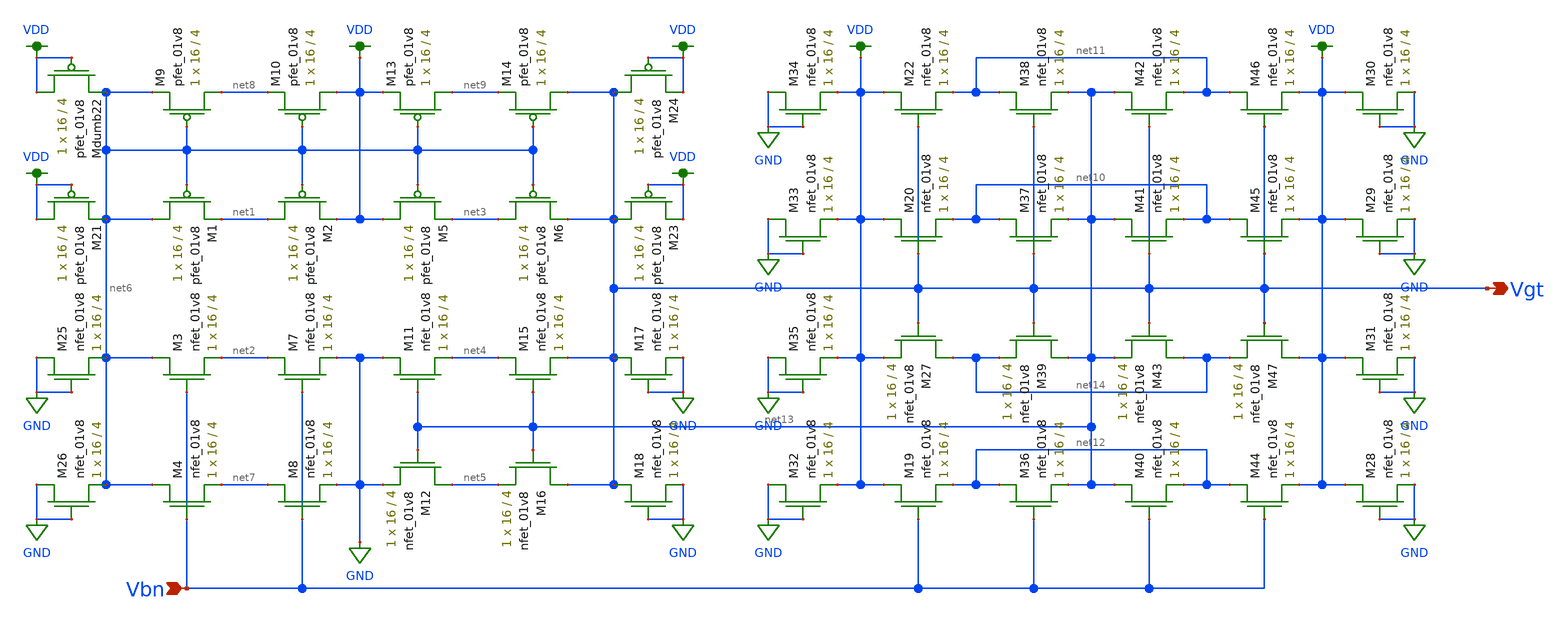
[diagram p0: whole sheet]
** sch_path: schematic/LDS/Vg_gen_lvs.sch
**.subckt Vg_gen_lvs Vbn Vgt
*.ipin Vbn
*.opin Vgt
XM1 net6 net6 net1 VDD sky130_fd_pr__pfet_01v8 L=4 W=16 nf=1 ad='int((nf+1)/2) * W/nf * 0.29' as='int((nf+2)/2) * W/nf * 0.29'
+ pd='2*int((nf+1)/2) * (W/nf + 0.29)' ps='2*int((nf+2)/2) * (W/nf + 0.29)' nrd='0.29 / W' nrs='0.29 / W'
+ sa=0 sb=0 sd=0 mult=1 m=1
XM2 net1 net6 VDD VDD sky130_fd_pr__pfet_01v8 L=4 W=16 nf=1 ad='int((nf+1)/2) * W/nf * 0.29' as='int((nf+2)/2) * W/nf * 0.29'
+ pd='2*int((nf+1)/2) * (W/nf + 0.29)' ps='2*int((nf+2)/2) * (W/nf + 0.29)' nrd='0.29 / W' nrs='0.29 / W'
+ sa=0 sb=0 sd=0 mult=1 m=1
XM5 VDD net6 net3 VDD sky130_fd_pr__pfet_01v8 L=4 W=16 nf=1 ad='int((nf+1)/2) * W/nf * 0.29' as='int((nf+2)/2) * W/nf * 0.29'
+ pd='2*int((nf+1)/2) * (W/nf + 0.29)' ps='2*int((nf+2)/2) * (W/nf + 0.29)' nrd='0.29 / W' nrs='0.29 / W'
+ sa=0 sb=0 sd=0 mult=1 m=1
XM6 net3 net6 Vgt VDD sky130_fd_pr__pfet_01v8 L=4 W=16 nf=1 ad='int((nf+1)/2) * W/nf * 0.29' as='int((nf+2)/2) * W/nf * 0.29'
+ pd='2*int((nf+1)/2) * (W/nf + 0.29)' ps='2*int((nf+2)/2) * (W/nf + 0.29)' nrd='0.29 / W' nrs='0.29 / W'
+ sa=0 sb=0 sd=0 mult=1 m=1
XM9 net8 net6 net6 VDD sky130_fd_pr__pfet_01v8 L=4 W=16 nf=1 ad='int((nf+1)/2) * W/nf * 0.29' as='int((nf+2)/2) * W/nf * 0.29'
+ pd='2*int((nf+1)/2) * (W/nf + 0.29)' ps='2*int((nf+2)/2) * (W/nf + 0.29)' nrd='0.29 / W' nrs='0.29 / W'
+ sa=0 sb=0 sd=0 mult=1 m=1
XM10 VDD net6 net8 VDD sky130_fd_pr__pfet_01v8 L=4 W=16 nf=1 ad='int((nf+1)/2) * W/nf * 0.29' as='int((nf+2)/2) * W/nf * 0.29'
+ pd='2*int((nf+1)/2) * (W/nf + 0.29)' ps='2*int((nf+2)/2) * (W/nf + 0.29)' nrd='0.29 / W' nrs='0.29 / W'
+ sa=0 sb=0 sd=0 mult=1 m=1
XM13 net9 net6 VDD VDD sky130_fd_pr__pfet_01v8 L=4 W=16 nf=1 ad='int((nf+1)/2) * W/nf * 0.29' as='int((nf+2)/2) * W/nf * 0.29'
+ pd='2*int((nf+1)/2) * (W/nf + 0.29)' ps='2*int((nf+2)/2) * (W/nf + 0.29)' nrd='0.29 / W' nrs='0.29 / W'
+ sa=0 sb=0 sd=0 mult=1 m=1
XM14 Vgt net6 net9 VDD sky130_fd_pr__pfet_01v8 L=4 W=16 nf=1 ad='int((nf+1)/2) * W/nf * 0.29' as='int((nf+2)/2) * W/nf * 0.29'
+ pd='2*int((nf+1)/2) * (W/nf + 0.29)' ps='2*int((nf+2)/2) * (W/nf + 0.29)' nrd='0.29 / W' nrs='0.29 / W'
+ sa=0 sb=0 sd=0 mult=1 m=1
XM21 VDD VDD net6 VDD sky130_fd_pr__pfet_01v8 L=4 W=16 nf=1 ad='int((nf+1)/2) * W/nf * 0.29' as='int((nf+2)/2) * W/nf * 0.29'
+ pd='2*int((nf+1)/2) * (W/nf + 0.29)' ps='2*int((nf+2)/2) * (W/nf + 0.29)' nrd='0.29 / W' nrs='0.29 / W'
+ sa=0 sb=0 sd=0 mult=1 m=1
XMdumb22 VDD VDD net6 VDD sky130_fd_pr__pfet_01v8 L=4 W=16 nf=1 ad='int((nf+1)/2) * W/nf * 0.29' as='int((nf+2)/2) * W/nf * 0.29'
+ pd='2*int((nf+1)/2) * (W/nf + 0.29)' ps='2*int((nf+2)/2) * (W/nf + 0.29)' nrd='0.29 / W' nrs='0.29 / W'
+ sa=0 sb=0 sd=0 mult=1 m=1
XM23 Vgt VDD VDD VDD sky130_fd_pr__pfet_01v8 L=4 W=16 nf=1 ad='int((nf+1)/2) * W/nf * 0.29' as='int((nf+2)/2) * W/nf * 0.29'
+ pd='2*int((nf+1)/2) * (W/nf + 0.29)' ps='2*int((nf+2)/2) * (W/nf + 0.29)' nrd='0.29 / W' nrs='0.29 / W'
+ sa=0 sb=0 sd=0 mult=1 m=1
XM24 Vgt VDD VDD VDD sky130_fd_pr__pfet_01v8 L=4 W=16 nf=1 ad='int((nf+1)/2) * W/nf * 0.29' as='int((nf+2)/2) * W/nf * 0.29'
+ pd='2*int((nf+1)/2) * (W/nf + 0.29)' ps='2*int((nf+2)/2) * (W/nf + 0.29)' nrd='0.29 / W' nrs='0.29 / W'
+ sa=0 sb=0 sd=0 mult=1 m=1
XM25 GND GND net6 GND sky130_fd_pr__nfet_01v8 L=4 W=16 nf=1 ad='int((nf+1)/2) * W/nf * 0.29' as='int((nf+2)/2) * W/nf * 0.29'
+ pd='2*int((nf+1)/2) * (W/nf + 0.29)' ps='2*int((nf+2)/2) * (W/nf + 0.29)' nrd='0.29 / W' nrs='0.29 / W'
+ sa=0 sb=0 sd=0 mult=1 m=1
XM26 GND GND net6 GND sky130_fd_pr__nfet_01v8 L=4 W=16 nf=1 ad='int((nf+1)/2) * W/nf * 0.29' as='int((nf+2)/2) * W/nf * 0.29'
+ pd='2*int((nf+1)/2) * (W/nf + 0.29)' ps='2*int((nf+2)/2) * (W/nf + 0.29)' nrd='0.29 / W' nrs='0.29 / W'
+ sa=0 sb=0 sd=0 mult=1 m=1
XM3 net6 Vbn net2 GND sky130_fd_pr__nfet_01v8 L=4 W=16 nf=1 ad='int((nf+1)/2) * W/nf * 0.29' as='int((nf+2)/2) * W/nf * 0.29'
+ pd='2*int((nf+1)/2) * (W/nf + 0.29)' ps='2*int((nf+2)/2) * (W/nf + 0.29)' nrd='0.29 / W' nrs='0.29 / W'
+ sa=0 sb=0 sd=0 mult=1 m=1
XM4 net6 Vbn net7 GND sky130_fd_pr__nfet_01v8 L=4 W=16 nf=1 ad='int((nf+1)/2) * W/nf * 0.29' as='int((nf+2)/2) * W/nf * 0.29'
+ pd='2*int((nf+1)/2) * (W/nf + 0.29)' ps='2*int((nf+2)/2) * (W/nf + 0.29)' nrd='0.29 / W' nrs='0.29 / W'
+ sa=0 sb=0 sd=0 mult=1 m=1
XM7 net2 Vbn GND GND sky130_fd_pr__nfet_01v8 L=4 W=16 nf=1 ad='int((nf+1)/2) * W/nf * 0.29' as='int((nf+2)/2) * W/nf * 0.29'
+ pd='2*int((nf+1)/2) * (W/nf + 0.29)' ps='2*int((nf+2)/2) * (W/nf + 0.29)' nrd='0.29 / W' nrs='0.29 / W'
+ sa=0 sb=0 sd=0 mult=1 m=1
XM8 net7 Vbn GND GND sky130_fd_pr__nfet_01v8 L=4 W=16 nf=1 ad='int((nf+1)/2) * W/nf * 0.29' as='int((nf+2)/2) * W/nf * 0.29'
+ pd='2*int((nf+1)/2) * (W/nf + 0.29)' ps='2*int((nf+2)/2) * (W/nf + 0.29)' nrd='0.29 / W' nrs='0.29 / W'
+ sa=0 sb=0 sd=0 mult=1 m=1
XM11 GND net13 net4 GND sky130_fd_pr__nfet_01v8 L=4 W=16 nf=1 ad='int((nf+1)/2) * W/nf * 0.29' as='int((nf+2)/2) * W/nf * 0.29'
+ pd='2*int((nf+1)/2) * (W/nf + 0.29)' ps='2*int((nf+2)/2) * (W/nf + 0.29)' nrd='0.29 / W' nrs='0.29 / W'
+ sa=0 sb=0 sd=0 mult=1 m=1
XM12 net5 net13 GND GND sky130_fd_pr__nfet_01v8 L=4 W=16 nf=1 ad='int((nf+1)/2) * W/nf * 0.29' as='int((nf+2)/2) * W/nf * 0.29'
+ pd='2*int((nf+1)/2) * (W/nf + 0.29)' ps='2*int((nf+2)/2) * (W/nf + 0.29)' nrd='0.29 / W' nrs='0.29 / W'
+ sa=0 sb=0 sd=0 mult=1 m=1
XM15 net4 net13 Vgt GND sky130_fd_pr__nfet_01v8 L=4 W=16 nf=1 ad='int((nf+1)/2) * W/nf * 0.29' as='int((nf+2)/2) * W/nf * 0.29'
+ pd='2*int((nf+1)/2) * (W/nf + 0.29)' ps='2*int((nf+2)/2) * (W/nf + 0.29)' nrd='0.29 / W' nrs='0.29 / W'
+ sa=0 sb=0 sd=0 mult=1 m=1
XM16 Vgt net13 net5 GND sky130_fd_pr__nfet_01v8 L=4 W=16 nf=1 ad='int((nf+1)/2) * W/nf * 0.29' as='int((nf+2)/2) * W/nf * 0.29'
+ pd='2*int((nf+1)/2) * (W/nf + 0.29)' ps='2*int((nf+2)/2) * (W/nf + 0.29)' nrd='0.29 / W' nrs='0.29 / W'
+ sa=0 sb=0 sd=0 mult=1 m=1
XM17 Vgt GND GND GND sky130_fd_pr__nfet_01v8 L=4 W=16 nf=1 ad='int((nf+1)/2) * W/nf * 0.29' as='int((nf+2)/2) * W/nf * 0.29'
+ pd='2*int((nf+1)/2) * (W/nf + 0.29)' ps='2*int((nf+2)/2) * (W/nf + 0.29)' nrd='0.29 / W' nrs='0.29 / W'
+ sa=0 sb=0 sd=0 mult=1 m=1
XM18 Vgt GND GND GND sky130_fd_pr__nfet_01v8 L=4 W=16 nf=1 ad='int((nf+1)/2) * W/nf * 0.29' as='int((nf+2)/2) * W/nf * 0.29'
+ pd='2*int((nf+1)/2) * (W/nf + 0.29)' ps='2*int((nf+2)/2) * (W/nf + 0.29)' nrd='0.29 / W' nrs='0.29 / W'
+ sa=0 sb=0 sd=0 mult=1 m=1
XM19 VDD Vbn net12 GND sky130_fd_pr__nfet_01v8 L=4 W=16 nf=1 ad='int((nf+1)/2) * W/nf * 0.29' as='int((nf+2)/2) * W/nf * 0.29'
+ pd='2*int((nf+1)/2) * (W/nf + 0.29)' ps='2*int((nf+2)/2) * (W/nf + 0.29)' nrd='0.29 / W' nrs='0.29 / W'
+ sa=0 sb=0 sd=0 mult=1 m=1
XM20 VDD Vgt net10 GND sky130_fd_pr__nfet_01v8 L=4 W=16 nf=1 ad='int((nf+1)/2) * W/nf * 0.29' as='int((nf+2)/2) * W/nf * 0.29'
+ pd='2*int((nf+1)/2) * (W/nf + 0.29)' ps='2*int((nf+2)/2) * (W/nf + 0.29)' nrd='0.29 / W' nrs='0.29 / W'
+ sa=0 sb=0 sd=0 mult=1 m=1
XM22 VDD Vgt net11 GND sky130_fd_pr__nfet_01v8 L=4 W=16 nf=1 ad='int((nf+1)/2) * W/nf * 0.29' as='int((nf+2)/2) * W/nf * 0.29'
+ pd='2*int((nf+1)/2) * (W/nf + 0.29)' ps='2*int((nf+2)/2) * (W/nf + 0.29)' nrd='0.29 / W' nrs='0.29 / W'
+ sa=0 sb=0 sd=0 mult=1 m=1
XM27 net14 Vgt VDD GND sky130_fd_pr__nfet_01v8 L=4 W=16 nf=1 ad='int((nf+1)/2) * W/nf * 0.29' as='int((nf+2)/2) * W/nf * 0.29'
+ pd='2*int((nf+1)/2) * (W/nf + 0.29)' ps='2*int((nf+2)/2) * (W/nf + 0.29)' nrd='0.29 / W' nrs='0.29 / W'
+ sa=0 sb=0 sd=0 mult=1 m=1
XM28 VDD GND GND GND sky130_fd_pr__nfet_01v8 L=4 W=16 nf=1 ad='int((nf+1)/2) * W/nf * 0.29' as='int((nf+2)/2) * W/nf * 0.29'
+ pd='2*int((nf+1)/2) * (W/nf + 0.29)' ps='2*int((nf+2)/2) * (W/nf + 0.29)' nrd='0.29 / W' nrs='0.29 / W'
+ sa=0 sb=0 sd=0 mult=1 m=1
XM29 VDD GND GND GND sky130_fd_pr__nfet_01v8 L=4 W=16 nf=1 ad='int((nf+1)/2) * W/nf * 0.29' as='int((nf+2)/2) * W/nf * 0.29'
+ pd='2*int((nf+1)/2) * (W/nf + 0.29)' ps='2*int((nf+2)/2) * (W/nf + 0.29)' nrd='0.29 / W' nrs='0.29 / W'
+ sa=0 sb=0 sd=0 mult=1 m=1
XM30 VDD GND GND GND sky130_fd_pr__nfet_01v8 L=4 W=16 nf=1 ad='int((nf+1)/2) * W/nf * 0.29' as='int((nf+2)/2) * W/nf * 0.29'
+ pd='2*int((nf+1)/2) * (W/nf + 0.29)' ps='2*int((nf+2)/2) * (W/nf + 0.29)' nrd='0.29 / W' nrs='0.29 / W'
+ sa=0 sb=0 sd=0 mult=1 m=1
XM31 VDD GND GND GND sky130_fd_pr__nfet_01v8 L=4 W=16 nf=1 ad='int((nf+1)/2) * W/nf * 0.29' as='int((nf+2)/2) * W/nf * 0.29'
+ pd='2*int((nf+1)/2) * (W/nf + 0.29)' ps='2*int((nf+2)/2) * (W/nf + 0.29)' nrd='0.29 / W' nrs='0.29 / W'
+ sa=0 sb=0 sd=0 mult=1 m=1
XM32 GND GND VDD GND sky130_fd_pr__nfet_01v8 L=4 W=16 nf=1 ad='int((nf+1)/2) * W/nf * 0.29' as='int((nf+2)/2) * W/nf * 0.29'
+ pd='2*int((nf+1)/2) * (W/nf + 0.29)' ps='2*int((nf+2)/2) * (W/nf + 0.29)' nrd='0.29 / W' nrs='0.29 / W'
+ sa=0 sb=0 sd=0 mult=1 m=1
XM33 GND GND VDD GND sky130_fd_pr__nfet_01v8 L=4 W=16 nf=1 ad='int((nf+1)/2) * W/nf * 0.29' as='int((nf+2)/2) * W/nf * 0.29'
+ pd='2*int((nf+1)/2) * (W/nf + 0.29)' ps='2*int((nf+2)/2) * (W/nf + 0.29)' nrd='0.29 / W' nrs='0.29 / W'
+ sa=0 sb=0 sd=0 mult=1 m=1
XM34 GND GND VDD GND sky130_fd_pr__nfet_01v8 L=4 W=16 nf=1 ad='int((nf+1)/2) * W/nf * 0.29' as='int((nf+2)/2) * W/nf * 0.29'
+ pd='2*int((nf+1)/2) * (W/nf + 0.29)' ps='2*int((nf+2)/2) * (W/nf + 0.29)' nrd='0.29 / W' nrs='0.29 / W'
+ sa=0 sb=0 sd=0 mult=1 m=1
XM35 GND GND VDD GND sky130_fd_pr__nfet_01v8 L=4 W=16 nf=1 ad='int((nf+1)/2) * W/nf * 0.29' as='int((nf+2)/2) * W/nf * 0.29'
+ pd='2*int((nf+1)/2) * (W/nf + 0.29)' ps='2*int((nf+2)/2) * (W/nf + 0.29)' nrd='0.29 / W' nrs='0.29 / W'
+ sa=0 sb=0 sd=0 mult=1 m=1
XM36 net12 Vbn net13 GND sky130_fd_pr__nfet_01v8 L=4 W=16 nf=1 ad='int((nf+1)/2) * W/nf * 0.29' as='int((nf+2)/2) * W/nf * 0.29'
+ pd='2*int((nf+1)/2) * (W/nf + 0.29)' ps='2*int((nf+2)/2) * (W/nf + 0.29)' nrd='0.29 / W' nrs='0.29 / W'
+ sa=0 sb=0 sd=0 mult=1 m=1
XM37 net10 Vgt net13 GND sky130_fd_pr__nfet_01v8 L=4 W=16 nf=1 ad='int((nf+1)/2) * W/nf * 0.29' as='int((nf+2)/2) * W/nf * 0.29'
+ pd='2*int((nf+1)/2) * (W/nf + 0.29)' ps='2*int((nf+2)/2) * (W/nf + 0.29)' nrd='0.29 / W' nrs='0.29 / W'
+ sa=0 sb=0 sd=0 mult=1 m=1
XM38 net11 Vgt net13 GND sky130_fd_pr__nfet_01v8 L=4 W=16 nf=1 ad='int((nf+1)/2) * W/nf * 0.29' as='int((nf+2)/2) * W/nf * 0.29'
+ pd='2*int((nf+1)/2) * (W/nf + 0.29)' ps='2*int((nf+2)/2) * (W/nf + 0.29)' nrd='0.29 / W' nrs='0.29 / W'
+ sa=0 sb=0 sd=0 mult=1 m=1
XM39 net13 Vgt net14 GND sky130_fd_pr__nfet_01v8 L=4 W=16 nf=1 ad='int((nf+1)/2) * W/nf * 0.29' as='int((nf+2)/2) * W/nf * 0.29'
+ pd='2*int((nf+1)/2) * (W/nf + 0.29)' ps='2*int((nf+2)/2) * (W/nf + 0.29)' nrd='0.29 / W' nrs='0.29 / W'
+ sa=0 sb=0 sd=0 mult=1 m=1
XM40 net13 Vbn net12 GND sky130_fd_pr__nfet_01v8 L=4 W=16 nf=1 ad='int((nf+1)/2) * W/nf * 0.29' as='int((nf+2)/2) * W/nf * 0.29'
+ pd='2*int((nf+1)/2) * (W/nf + 0.29)' ps='2*int((nf+2)/2) * (W/nf + 0.29)' nrd='0.29 / W' nrs='0.29 / W'
+ sa=0 sb=0 sd=0 mult=1 m=1
XM41 net13 Vgt net10 GND sky130_fd_pr__nfet_01v8 L=4 W=16 nf=1 ad='int((nf+1)/2) * W/nf * 0.29' as='int((nf+2)/2) * W/nf * 0.29'
+ pd='2*int((nf+1)/2) * (W/nf + 0.29)' ps='2*int((nf+2)/2) * (W/nf + 0.29)' nrd='0.29 / W' nrs='0.29 / W'
+ sa=0 sb=0 sd=0 mult=1 m=1
XM42 net13 Vgt net11 GND sky130_fd_pr__nfet_01v8 L=4 W=16 nf=1 ad='int((nf+1)/2) * W/nf * 0.29' as='int((nf+2)/2) * W/nf * 0.29'
+ pd='2*int((nf+1)/2) * (W/nf + 0.29)' ps='2*int((nf+2)/2) * (W/nf + 0.29)' nrd='0.29 / W' nrs='0.29 / W'
+ sa=0 sb=0 sd=0 mult=1 m=1
XM43 net14 Vgt net13 GND sky130_fd_pr__nfet_01v8 L=4 W=16 nf=1 ad='int((nf+1)/2) * W/nf * 0.29' as='int((nf+2)/2) * W/nf * 0.29'
+ pd='2*int((nf+1)/2) * (W/nf + 0.29)' ps='2*int((nf+2)/2) * (W/nf + 0.29)' nrd='0.29 / W' nrs='0.29 / W'
+ sa=0 sb=0 sd=0 mult=1 m=1
XM44 net12 Vbn VDD GND sky130_fd_pr__nfet_01v8 L=4 W=16 nf=1 ad='int((nf+1)/2) * W/nf * 0.29' as='int((nf+2)/2) * W/nf * 0.29'
+ pd='2*int((nf+1)/2) * (W/nf + 0.29)' ps='2*int((nf+2)/2) * (W/nf + 0.29)' nrd='0.29 / W' nrs='0.29 / W'
+ sa=0 sb=0 sd=0 mult=1 m=1
XM45 net10 Vgt VDD GND sky130_fd_pr__nfet_01v8 L=4 W=16 nf=1 ad='int((nf+1)/2) * W/nf * 0.29' as='int((nf+2)/2) * W/nf * 0.29'
+ pd='2*int((nf+1)/2) * (W/nf + 0.29)' ps='2*int((nf+2)/2) * (W/nf + 0.29)' nrd='0.29 / W' nrs='0.29 / W'
+ sa=0 sb=0 sd=0 mult=1 m=1
XM46 net11 Vgt VDD GND sky130_fd_pr__nfet_01v8 L=4 W=16 nf=1 ad='int((nf+1)/2) * W/nf * 0.29' as='int((nf+2)/2) * W/nf * 0.29'
+ pd='2*int((nf+1)/2) * (W/nf + 0.29)' ps='2*int((nf+2)/2) * (W/nf + 0.29)' nrd='0.29 / W' nrs='0.29 / W'
+ sa=0 sb=0 sd=0 mult=1 m=1
XM47 VDD Vgt net14 GND sky130_fd_pr__nfet_01v8 L=4 W=16 nf=1 ad='int((nf+1)/2) * W/nf * 0.29' as='int((nf+2)/2) * W/nf * 0.29'
+ pd='2*int((nf+1)/2) * (W/nf + 0.29)' ps='2*int((nf+2)/2) * (W/nf + 0.29)' nrd='0.29 / W' nrs='0.29 / W'
+ sa=0 sb=0 sd=0 mult=1 m=1
**.ends
.GLOBAL GND
.GLOBAL VDD
.end
